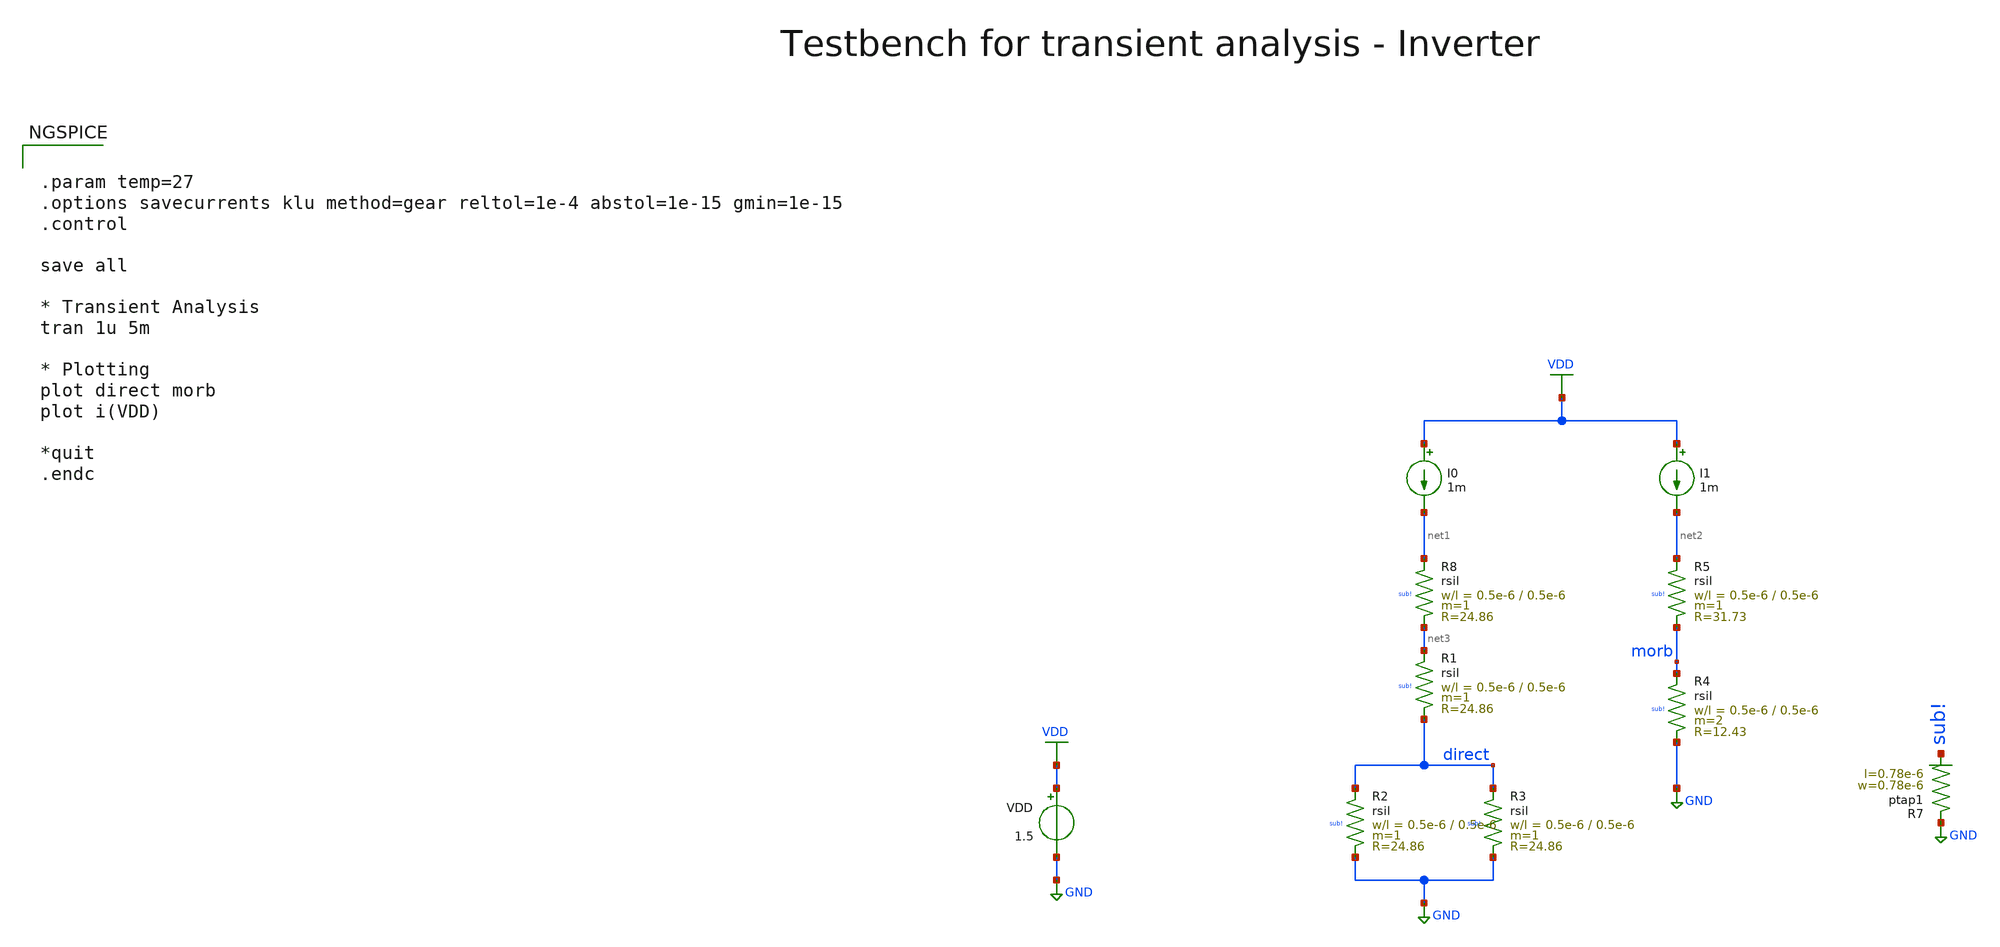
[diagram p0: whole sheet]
** sch_path: multiplier_support/testbench/rsil_tb_tran.sch
**.subckt rsil_tb_tran
VDD VDD GND 1.5
I0 VDD net1 1m
I1 VDD net2 1m
XR7 GND sub! ptap1 R=262.8 w=0.78e-6 l=0.78e-6
XR8 net1 net3 sub! rsil w=0.5e-6 l=0.5e-6 m=1 mm_ok=1
XR1 net3 direct sub! rsil w=0.5e-6 l=0.5e-6 m=1 mm_ok=1
XR2 direct GND sub! rsil w=0.5e-6 l=0.5e-6 m=1 mm_ok=1
XR3 direct GND sub! rsil w=0.5e-6 l=0.5e-6 m=1 mm_ok=1
XR4 morb GND sub! rsil w=0.5e-6 l=0.5e-6 m=2 mm_ok=1
XR5 net2 morb sub! rsil w=0.5e-6 l=0.5e-6 m=1 mm_ok=1
**** begin user architecture code


.param temp=27
.options savecurrents klu method=gear reltol=1e-4 abstol=1e-15 gmin=1e-15
.control

save all

* Transient Analysis
tran 1u 5m

* Plotting
plot direct morb
plot i(VDD)

*quit
.endc



.lib cornerMOSlv.lib mos_tt
.lib cornerMOShv.lib mos_tt
.lib cornerHBT.lib hbt_typ
.lib cornerRES.lib res_typ
.lib cornerCAP.lib cap_typ
.lib cornerDIO.lib dio_tt

**** end user architecture code
**.ends
.GLOBAL GND
.GLOBAL VDD
.end
